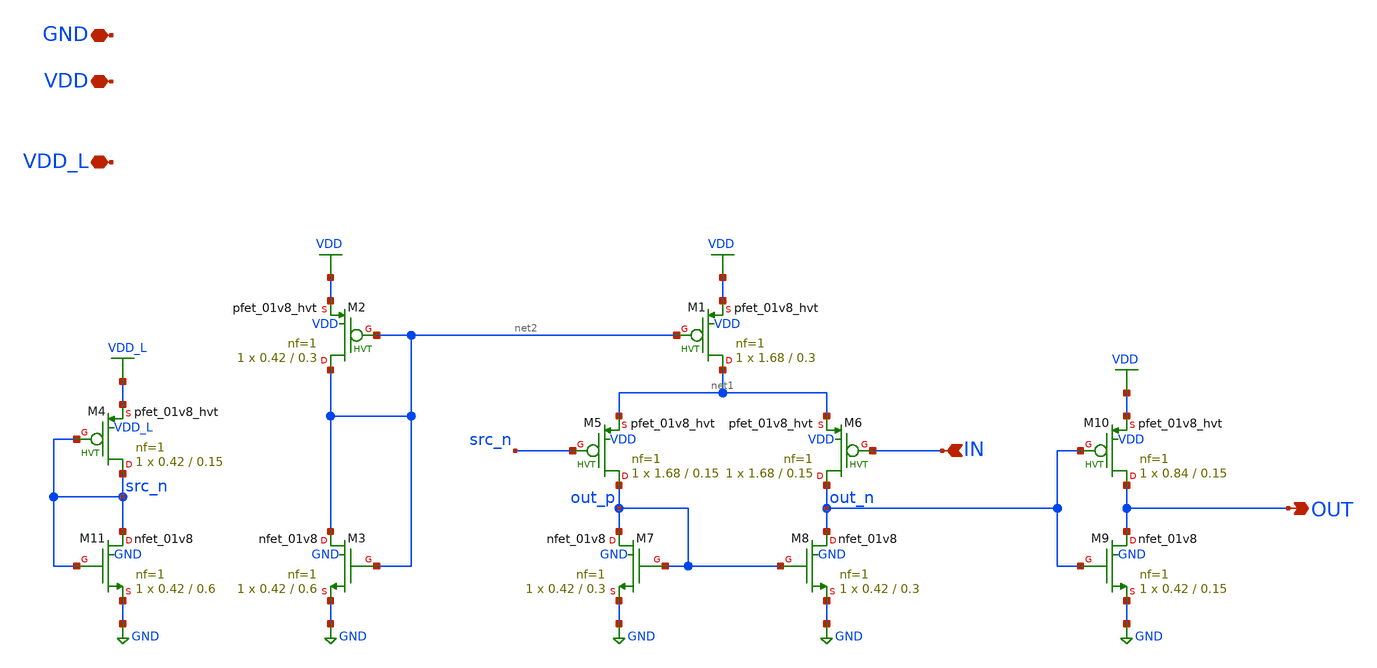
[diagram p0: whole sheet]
** sch_path: xschem/level_shifter2.sch
**.subckt level_shifter2 VDD_L VDD GND IN OUT
*.iopin VDD_L
*.iopin VDD
*.iopin GND
*.ipin IN
*.opin OUT
XM5 out_p src_n net1 VDD sky130_fd_pr__pfet_01v8_hvt L=0.15 W=1.68 nf=1 ad='int((nf+1)/2) * W/nf * 0.29'
+ as='int((nf+2)/2) * W/nf * 0.29' pd='2*int((nf+1)/2) * (W/nf + 0.29)' ps='2*int((nf+2)/2) * (W/nf + 0.29)'
+ nrd='0.29 / W' nrs='0.29 / W' sa=0 sb=0 sd=0 mult=1 m=1
XM6 out_n IN net1 VDD sky130_fd_pr__pfet_01v8_hvt L=0.15 W=1.68 nf=1 ad='int((nf+1)/2) * W/nf * 0.29'
+ as='int((nf+2)/2) * W/nf * 0.29' pd='2*int((nf+1)/2) * (W/nf + 0.29)' ps='2*int((nf+2)/2) * (W/nf + 0.29)'
+ nrd='0.29 / W' nrs='0.29 / W' sa=0 sb=0 sd=0 mult=1 m=1
XM7 out_p out_p GND GND sky130_fd_pr__nfet_01v8 L=0.3 W=0.42 nf=1 ad='int((nf+1)/2) * W/nf * 0.29' as='int((nf+2)/2) * W/nf * 0.29'
+ pd='2*int((nf+1)/2) * (W/nf + 0.29)' ps='2*int((nf+2)/2) * (W/nf + 0.29)' nrd='0.29 / W' nrs='0.29 / W'
+ sa=0 sb=0 sd=0 mult=1 m=1
XM8 out_n out_p GND GND sky130_fd_pr__nfet_01v8 L=0.3 W=0.42 nf=1 ad='int((nf+1)/2) * W/nf * 0.29' as='int((nf+2)/2) * W/nf * 0.29'
+ pd='2*int((nf+1)/2) * (W/nf + 0.29)' ps='2*int((nf+2)/2) * (W/nf + 0.29)' nrd='0.29 / W' nrs='0.29 / W'
+ sa=0 sb=0 sd=0 mult=1 m=1
XM9 OUT out_n GND GND sky130_fd_pr__nfet_01v8 L=0.15 W=0.42 nf=1 ad='int((nf+1)/2) * W/nf * 0.29' as='int((nf+2)/2) * W/nf * 0.29'
+ pd='2*int((nf+1)/2) * (W/nf + 0.29)' ps='2*int((nf+2)/2) * (W/nf + 0.29)' nrd='0.29 / W' nrs='0.29 / W'
+ sa=0 sb=0 sd=0 mult=1 m=1
XM10 OUT out_n VDD VDD sky130_fd_pr__pfet_01v8_hvt L=0.15 W=0.84 nf=1 ad='int((nf+1)/2) * W/nf * 0.29'
+ as='int((nf+2)/2) * W/nf * 0.29' pd='2*int((nf+1)/2) * (W/nf + 0.29)' ps='2*int((nf+2)/2) * (W/nf + 0.29)'
+ nrd='0.29 / W' nrs='0.29 / W' sa=0 sb=0 sd=0 mult=1 m=1
XM1 net1 net2 VDD VDD sky130_fd_pr__pfet_01v8_hvt L=0.3 W=1.68 nf=1 ad='int((nf+1)/2) * W/nf * 0.29'
+ as='int((nf+2)/2) * W/nf * 0.29' pd='2*int((nf+1)/2) * (W/nf + 0.29)' ps='2*int((nf+2)/2) * (W/nf + 0.29)'
+ nrd='0.29 / W' nrs='0.29 / W' sa=0 sb=0 sd=0 mult=1 m=1
XM2 net2 net2 VDD VDD sky130_fd_pr__pfet_01v8_hvt L=0.3 W=0.42 nf=1 ad='int((nf+1)/2) * W/nf * 0.29'
+ as='int((nf+2)/2) * W/nf * 0.29' pd='2*int((nf+1)/2) * (W/nf + 0.29)' ps='2*int((nf+2)/2) * (W/nf + 0.29)'
+ nrd='0.29 / W' nrs='0.29 / W' sa=0 sb=0 sd=0 mult=1 m=1
XM3 net2 net2 GND GND sky130_fd_pr__nfet_01v8 L=0.6 W=0.42 nf=1 ad='int((nf+1)/2) * W/nf * 0.29' as='int((nf+2)/2) * W/nf * 0.29'
+ pd='2*int((nf+1)/2) * (W/nf + 0.29)' ps='2*int((nf+2)/2) * (W/nf + 0.29)' nrd='0.29 / W' nrs='0.29 / W'
+ sa=0 sb=0 sd=0 mult=1 m=1
XM4 src_n src_n VDD_L VDD_L sky130_fd_pr__pfet_01v8_hvt L=0.15 W=0.42 nf=1 ad='int((nf+1)/2) * W/nf * 0.29'
+ as='int((nf+2)/2) * W/nf * 0.29' pd='2*int((nf+1)/2) * (W/nf + 0.29)' ps='2*int((nf+2)/2) * (W/nf + 0.29)'
+ nrd='0.29 / W' nrs='0.29 / W' sa=0 sb=0 sd=0 mult=1 m=1
XM11 src_n src_n GND GND sky130_fd_pr__nfet_01v8 L=0.6 W=0.42 nf=1 ad='int((nf+1)/2) * W/nf * 0.29' as='int((nf+2)/2) * W/nf * 0.29'
+ pd='2*int((nf+1)/2) * (W/nf + 0.29)' ps='2*int((nf+2)/2) * (W/nf + 0.29)' nrd='0.29 / W' nrs='0.29 / W'
+ sa=0 sb=0 sd=0 mult=1 m=1
**.ends
.GLOBAL VDD
.GLOBAL GND
.GLOBAL VDD_L
.end
